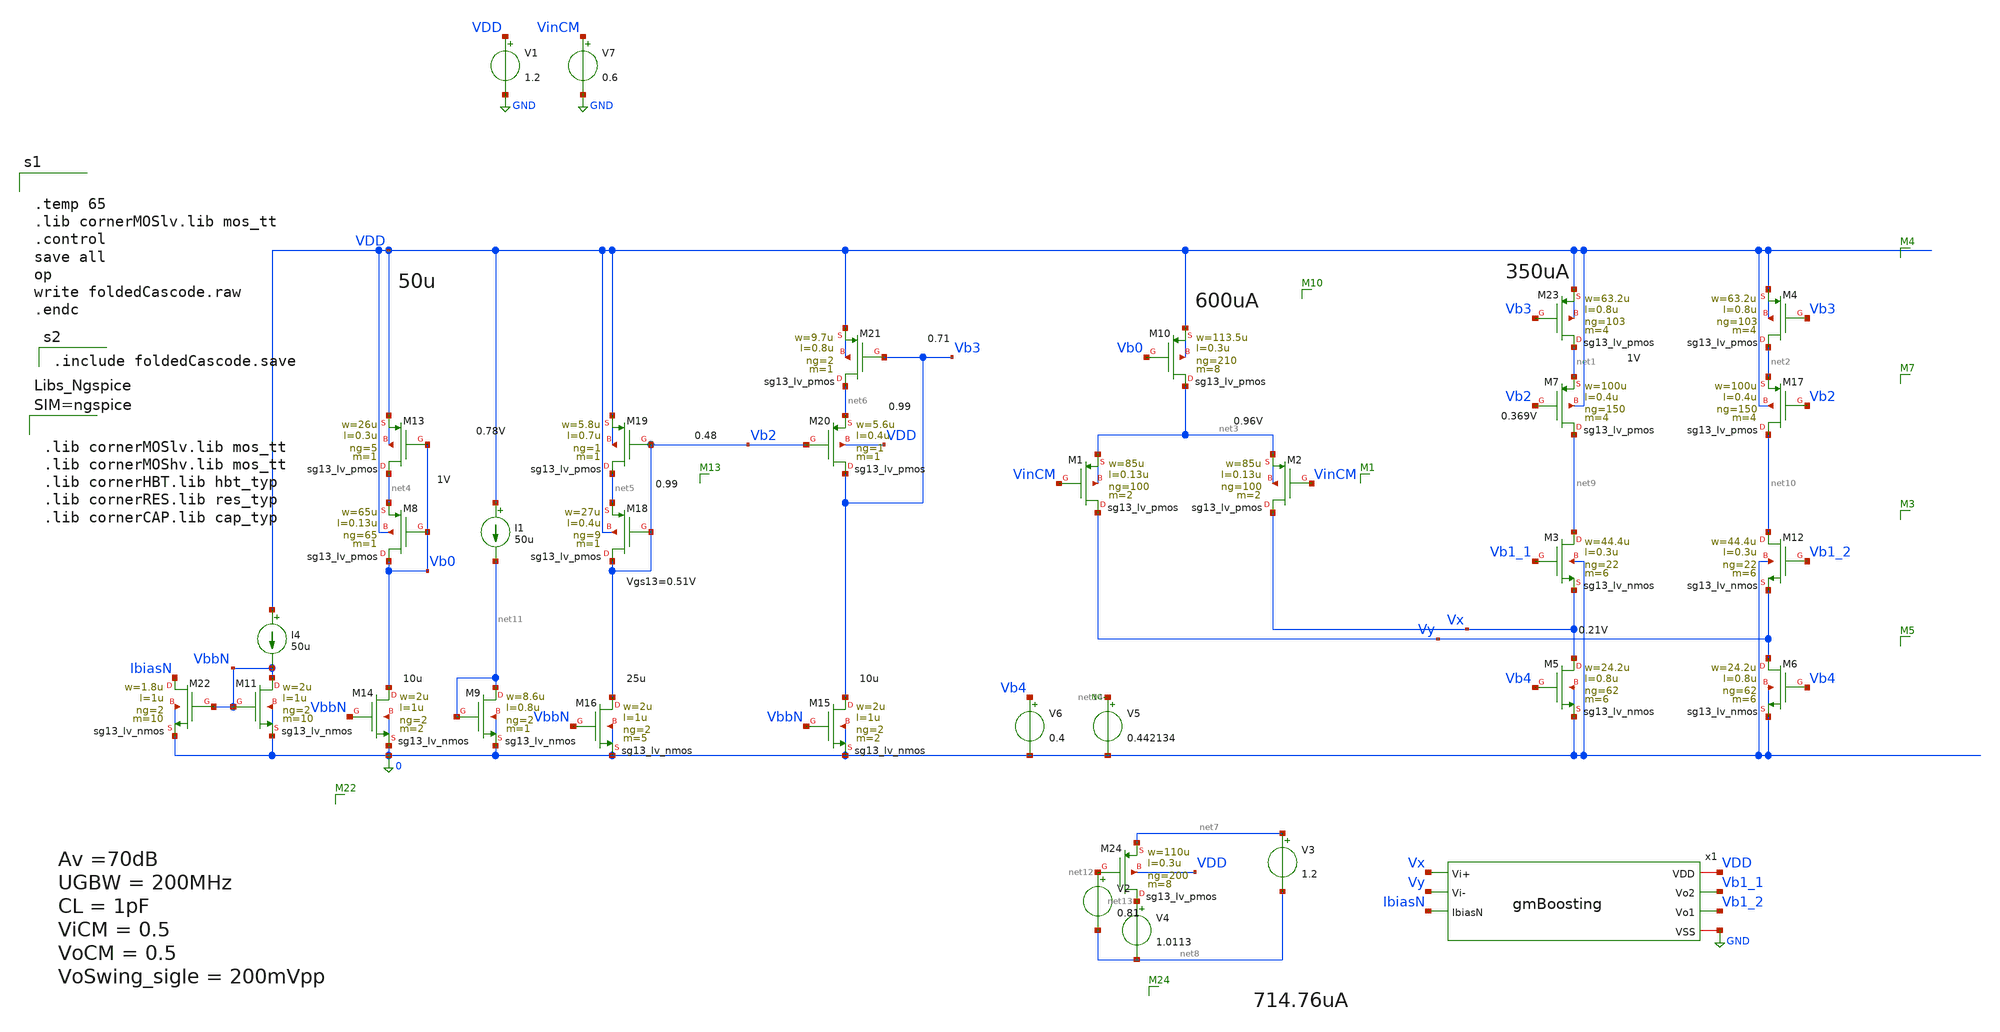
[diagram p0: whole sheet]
** sch_path: sch/testing/foldedCascode.sch
**.subckt foldedCascode
V1 VDD GND 1.2
XM5 Vx Vb4 0 0 sg13_lv_nmos w=24.2u l=0.8u ng=62 m=6 mm_ok=1
XM6 Vy Vb4 0 0 sg13_lv_nmos w=24.2u l=0.8u ng=62 m=6 mm_ok=1
V7 VinCM GND 0.6
XM1 Vy VinCM net3 net3 sg13_lv_pmos w=85u l=0.13u ng=100 m=2 mm_ok=1
x1 VDD Vb1_1 Vb1_2 Vx Vy GND IbiasN gmBoosting
XM2 Vx VinCM net3 net3 sg13_lv_pmos w=85u l=0.13u ng=100 m=2 mm_ok=1
V6 Vb4 0 0.4
XM3 net9 Vb1_1 Vx 0 sg13_lv_nmos w=44.4u l=0.3u ng=22 m=6 mm_ok=1
XM12 net10 Vb1_2 Vy 0 sg13_lv_nmos w=44.4u l=0.3u ng=22 m=6 mm_ok=1
XM8 Vb0 Vb0 net4 VDD sg13_lv_pmos w=65u l=0.13u ng=65 m=1 mm_ok=1
XM13 net4 Vb0 VDD VDD sg13_lv_pmos w=26u l=0.3u ng=5 m=1 mm_ok=1
XM18 Vb2 Vb2 net5 VDD sg13_lv_pmos w=27u l=0.4u ng=9 m=1 mm_ok=1
XM19 net5 Vb2 VDD VDD sg13_lv_pmos w=5.8u l=0.7u ng=1 m=1 mm_ok=1
XM20 Vb3 Vb2 net6 VDD sg13_lv_pmos w=5.6u l=0.4u ng=1 m=1 mm_ok=1
XM21 net6 Vb3 VDD VDD sg13_lv_pmos w=9.7u l=0.8u ng=2 m=1 mm_ok=1
XM11 VbbN VbbN 0 0 sg13_lv_nmos w=2u l=1u ng=2 m=10 mm_ok=1
I4 VDD VbbN 50u
XM14 Vb0 VbbN 0 0 sg13_lv_nmos w=2u l=1u ng=2 m=2 mm_ok=1
XM15 Vb3 VbbN 0 0 sg13_lv_nmos w=2u l=1u ng=2 m=2 mm_ok=1
XM16 Vb2 VbbN 0 0 sg13_lv_nmos w=2u l=1u ng=2 m=5 mm_ok=1
XM22 IbiasN VbbN 0 0 sg13_lv_nmos w=1.8u l=1u ng=2 m=10 mm_ok=1
V2 net12 net8 0.81
V3 net7 net8 1.2
V4 net13 net8 1.0113
XM17 net10 Vb2 net2 VDD sg13_lv_pmos w=100u l=0.4u ng=150 m=4 mm_ok=1
XM7 net9 Vb2 net1 VDD sg13_lv_pmos w=100u l=0.4u ng=150 m=4 mm_ok=1
XM23 net1 Vb3 VDD VDD sg13_lv_pmos w=63.2u l=0.8u ng=103 m=4 mm_ok=1
XM4 net2 Vb3 VDD VDD sg13_lv_pmos w=63.2u l=0.8u ng=103 m=4 mm_ok=1
I1 VDD net11 50u
XM9 net11 net11 0 0 sg13_lv_nmos w=8.6u l=0.8u ng=2 m=1 mm_ok=1
XM24 net13 net12 net7 VDD sg13_lv_pmos w=110u l=0.3u ng=200 m=8 mm_ok=1
V5 net14 0 0.442134
* noconn #net14
XM10 net3 Vb0 VDD VDD sg13_lv_pmos w=113.5u l=0.3u ng=210 m=8 mm_ok=1
**** begin user architecture code


.temp 65
.lib cornerMOSlv.lib mos_tt
.control
save all
op
write foldedCascode.raw
.endc



.include foldedCascode.save




.lib cornerMOSlv.lib mos_tt
.lib cornerMOShv.lib mos_tt
.lib cornerHBT.lib hbt_typ
.lib cornerRES.lib res_typ
.lib cornerCAP.lib cap_typ



**** end user architecture code
**.ends

* expanding   symbol:  gmBoosting.sym # of pins=7
** sym_path: sch/blocks/gmBoosting.sym
** sch_path: sch/blocks/gmBoosting.sch
.subckt gmBoosting VDD Vo2 Vo1 Vi+ Vi- VSS IbiasN
*.iopin VSS
*.opin Vo1
*.opin Vo2
*.ipin Vi+
*.ipin Vi-
*.iopin VDD
*.ipin IbiasN
XM7 net2 Vb4 VDD VDD sg13_lv_pmos w=19.8u l=0.7u ng=20 m=2 mm_ok=1
XM1 net7 Vi+ net1 net1 sg13_lv_pmos w=35u l=0.15u ng=70 m=4 mm_ok=1
XM2 net4 Vi- net1 net1 sg13_lv_pmos w=35u l=0.15u ng=70 m=4 mm_ok=1
XM0 net1 Vb0 net5 VDD sg13_lv_pmos w=12u l=0.3u ng=12 m=1 mm_ok=1
XM6 net7 Vb3 VSS VSS sg13_lv_nmos w=20.2u l=0.7u ng=5 m=2 mm_ok=1
XM9 Vo1 Vb2 net2 VDD sg13_lv_pmos w=23.2u l=0.3u ng=10 m=1 mm_ok=1
XM10 Vo2 Vb2 net3 VDD sg13_lv_pmos w=23.2u l=0.3u ng=10 m=1 mm_ok=1
XM3 net5 Vo2 VDD VDD sg13_lv_pmos w=20u l=0.13u ng=5 m=1 mm_ok=1
XM4 net5 Vo1 VDD VDD sg13_lv_pmos w=20u l=0.13u ng=5 m=1 mm_ok=1
XM5 net6 Va VDD VDD sg13_lv_pmos w=20u l=0.13u ng=5 m=2 mm_ok=1
XM29 Vb3 Vb3 VSS VSS sg13_lv_nmos w=32u l=0.7u ng=4 m=1 mm_ok=1
XM30 Vb3 Vb0 net6 VDD sg13_lv_pmos w=12u l=0.3u ng=12 m=1 mm_ok=1
XM31 net4 Vb3 VSS VSS sg13_lv_nmos w=20.2u l=0.7u ng=5 m=2 mm_ok=1
XM32 Vo1 Vb1 net4 VSS sg13_lv_nmos w=38.7u l=0.6u ng=5 m=1 mm_ok=1
XM21 IbiasN IbiasN VDD VDD sg13_lv_pmos w=18u l=1u ng=18 m=1 mm_ok=1
XM24 VbbN IbiasN VDD VDD sg13_lv_pmos w=18u l=1u ng=18 m=1 mm_ok=1
XM25 VbbN VbbN VSS VSS sg13_lv_nmos w=15u l=1u ng=2 m=1 mm_ok=1
XM17 Va VbbN VSS VSS sg13_lv_nmos w=15u l=1u ng=2 m=1 mm_ok=1
XM18 Va Va VDD VDD sg13_lv_pmos w=13u l=1u ng=13 m=1 mm_ok=1
XM19 Vb1 Vb1 net9 VSS sg13_lv_nmos w=13u l=0.7u ng=2 m=1 mm_ok=1
XM20 net9 Vb1 VSS VSS sg13_lv_nmos w=2.4u l=0.7u ng=1 m=1 mm_ok=1
XM22 Vb1 IbiasN VDD VDD sg13_lv_pmos w=18u l=1u ng=18 m=1 mm_ok=1
XM26 Vb4 Vb2 net8 VDD sg13_lv_pmos w=9u l=0.3u ng=9 m=1 mm_ok=1
XM38 net8 Vb4 VDD VDD sg13_lv_pmos w=15.5u l=0.7u ng=15 m=1 mm_ok=1
XM39 Vb4 VbbN VSS VSS sg13_lv_nmos w=15u l=1u ng=2 m=1 mm_ok=1
XM40 net11 Vb2 VDD VDD sg13_lv_pmos w=4.5u l=0.7u ng=1 m=1 mm_ok=1
XM41 Vb2 Vb2 net11 VDD sg13_lv_pmos w=15u l=0.7u ng=15 m=1 mm_ok=1
XM42 Vb2 VbbN VSS VSS sg13_lv_nmos w=15u l=1u ng=2 m=1 mm_ok=1
XM8 net3 Vb4 VDD VDD sg13_lv_pmos w=19.8u l=0.7u ng=20 m=2 mm_ok=1
XM11 Vo2 Vb1 net7 VSS sg13_lv_nmos w=38.7u l=0.6u ng=5 m=1 mm_ok=1
XM12 Vb0 VbbN VSS VSS sg13_lv_nmos w=15u l=1u ng=2 m=1 mm_ok=1
XM13 net10 Vb0 VDD VDD sg13_lv_pmos w=3.92u l=0.7u ng=2 m=1 mm_ok=1
XM14 Vb0 Vb0 net10 VDD sg13_lv_pmos w=55u l=0.15u ng=55 m=1 mm_ok=1
.ends

.GLOBAL GND
.end
